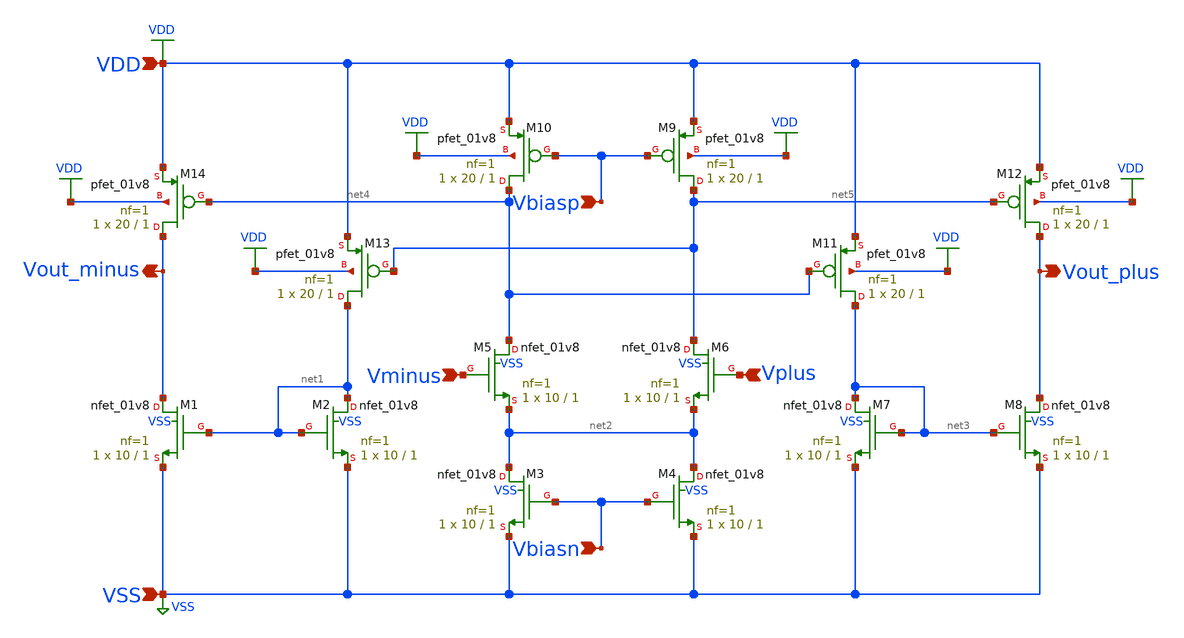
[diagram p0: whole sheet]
** sch_path: analog/schematics/DiffOpAmp.sch
**.subckt DiffOpAmp Vbiasn Vbiasp Vminus Vplus Vout_minus Vout_plus VDD VSS
*.ipin Vbiasn
*.ipin Vbiasp
*.ipin Vminus
*.ipin Vplus
*.opin Vout_minus
*.opin Vout_plus
*.ipin VDD
*.ipin VSS
XM1 Vout_minus net1 VSS VSS sky130_fd_pr__nfet_01v8 L=1 W=10 nf=1 ad='int((nf+1)/2) * W/nf * 0.29' as='int((nf+2)/2) * W/nf * 0.29'
+ pd='2*int((nf+1)/2) * (W/nf + 0.29)' ps='2*int((nf+2)/2) * (W/nf + 0.29)' nrd='0.29 / W' nrs='0.29 / W'
+ sa=0 sb=0 sd=0 mult=1 m=1
XM2 net1 net1 VSS VSS sky130_fd_pr__nfet_01v8 L=1 W=10 nf=1 ad='int((nf+1)/2) * W/nf * 0.29' as='int((nf+2)/2) * W/nf * 0.29'
+ pd='2*int((nf+1)/2) * (W/nf + 0.29)' ps='2*int((nf+2)/2) * (W/nf + 0.29)' nrd='0.29 / W' nrs='0.29 / W'
+ sa=0 sb=0 sd=0 mult=1 m=1
XM3 net2 Vbiasn VSS VSS sky130_fd_pr__nfet_01v8 L=1 W=10 nf=1 ad='int((nf+1)/2) * W/nf * 0.29' as='int((nf+2)/2) * W/nf * 0.29'
+ pd='2*int((nf+1)/2) * (W/nf + 0.29)' ps='2*int((nf+2)/2) * (W/nf + 0.29)' nrd='0.29 / W' nrs='0.29 / W'
+ sa=0 sb=0 sd=0 mult=1 m=1
XM4 net2 Vbiasn VSS VSS sky130_fd_pr__nfet_01v8 L=1 W=10 nf=1 ad='int((nf+1)/2) * W/nf * 0.29' as='int((nf+2)/2) * W/nf * 0.29'
+ pd='2*int((nf+1)/2) * (W/nf + 0.29)' ps='2*int((nf+2)/2) * (W/nf + 0.29)' nrd='0.29 / W' nrs='0.29 / W'
+ sa=0 sb=0 sd=0 mult=1 m=1
XM5 net4 Vminus net2 VSS sky130_fd_pr__nfet_01v8 L=1 W=10 nf=1 ad='int((nf+1)/2) * W/nf * 0.29' as='int((nf+2)/2) * W/nf * 0.29'
+ pd='2*int((nf+1)/2) * (W/nf + 0.29)' ps='2*int((nf+2)/2) * (W/nf + 0.29)' nrd='0.29 / W' nrs='0.29 / W'
+ sa=0 sb=0 sd=0 mult=1 m=1
XM6 net5 Vplus net2 VSS sky130_fd_pr__nfet_01v8 L=1 W=10 nf=1 ad='int((nf+1)/2) * W/nf * 0.29' as='int((nf+2)/2) * W/nf * 0.29'
+ pd='2*int((nf+1)/2) * (W/nf + 0.29)' ps='2*int((nf+2)/2) * (W/nf + 0.29)' nrd='0.29 / W' nrs='0.29 / W'
+ sa=0 sb=0 sd=0 mult=1 m=1
XM7 net3 net3 VSS VSS sky130_fd_pr__nfet_01v8 L=1 W=10 nf=1 ad='int((nf+1)/2) * W/nf * 0.29' as='int((nf+2)/2) * W/nf * 0.29'
+ pd='2*int((nf+1)/2) * (W/nf + 0.29)' ps='2*int((nf+2)/2) * (W/nf + 0.29)' nrd='0.29 / W' nrs='0.29 / W'
+ sa=0 sb=0 sd=0 mult=1 m=1
XM8 Vout_plus net3 VSS VSS sky130_fd_pr__nfet_01v8 L=1 W=10 nf=1 ad='int((nf+1)/2) * W/nf * 0.29' as='int((nf+2)/2) * W/nf * 0.29'
+ pd='2*int((nf+1)/2) * (W/nf + 0.29)' ps='2*int((nf+2)/2) * (W/nf + 0.29)' nrd='0.29 / W' nrs='0.29 / W'
+ sa=0 sb=0 sd=0 mult=1 m=1
XM9 net5 Vbiasp VDD VDD sky130_fd_pr__pfet_01v8 L=1 W=20 nf=1 ad='int((nf+1)/2) * W/nf * 0.29' as='int((nf+2)/2) * W/nf * 0.29'
+ pd='2*int((nf+1)/2) * (W/nf + 0.29)' ps='2*int((nf+2)/2) * (W/nf + 0.29)' nrd='0.29 / W' nrs='0.29 / W'
+ sa=0 sb=0 sd=0 mult=1 m=1
XM10 net4 Vbiasp VDD VDD sky130_fd_pr__pfet_01v8 L=1 W=20 nf=1 ad='int((nf+1)/2) * W/nf * 0.29' as='int((nf+2)/2) * W/nf * 0.29'
+ pd='2*int((nf+1)/2) * (W/nf + 0.29)' ps='2*int((nf+2)/2) * (W/nf + 0.29)' nrd='0.29 / W' nrs='0.29 / W'
+ sa=0 sb=0 sd=0 mult=1 m=1
XM11 net3 net4 VDD VDD sky130_fd_pr__pfet_01v8 L=1 W=20 nf=1 ad='int((nf+1)/2) * W/nf * 0.29' as='int((nf+2)/2) * W/nf * 0.29'
+ pd='2*int((nf+1)/2) * (W/nf + 0.29)' ps='2*int((nf+2)/2) * (W/nf + 0.29)' nrd='0.29 / W' nrs='0.29 / W'
+ sa=0 sb=0 sd=0 mult=1 m=1
XM12 Vout_plus net5 VDD VDD sky130_fd_pr__pfet_01v8 L=1 W=20 nf=1 ad='int((nf+1)/2) * W/nf * 0.29' as='int((nf+2)/2) * W/nf * 0.29'
+ pd='2*int((nf+1)/2) * (W/nf + 0.29)' ps='2*int((nf+2)/2) * (W/nf + 0.29)' nrd='0.29 / W' nrs='0.29 / W'
+ sa=0 sb=0 sd=0 mult=1 m=1
XM13 net1 net5 VDD VDD sky130_fd_pr__pfet_01v8 L=1 W=20 nf=1 ad='int((nf+1)/2) * W/nf * 0.29' as='int((nf+2)/2) * W/nf * 0.29'
+ pd='2*int((nf+1)/2) * (W/nf + 0.29)' ps='2*int((nf+2)/2) * (W/nf + 0.29)' nrd='0.29 / W' nrs='0.29 / W'
+ sa=0 sb=0 sd=0 mult=1 m=1
XM14 Vout_minus net4 VDD VDD sky130_fd_pr__pfet_01v8 L=1 W=20 nf=1 ad='int((nf+1)/2) * W/nf * 0.29' as='int((nf+2)/2) * W/nf * 0.29'
+ pd='2*int((nf+1)/2) * (W/nf + 0.29)' ps='2*int((nf+2)/2) * (W/nf + 0.29)' nrd='0.29 / W' nrs='0.29 / W'
+ sa=0 sb=0 sd=0 mult=1 m=1
**.ends
.GLOBAL VSS
.GLOBAL VDD
.end
